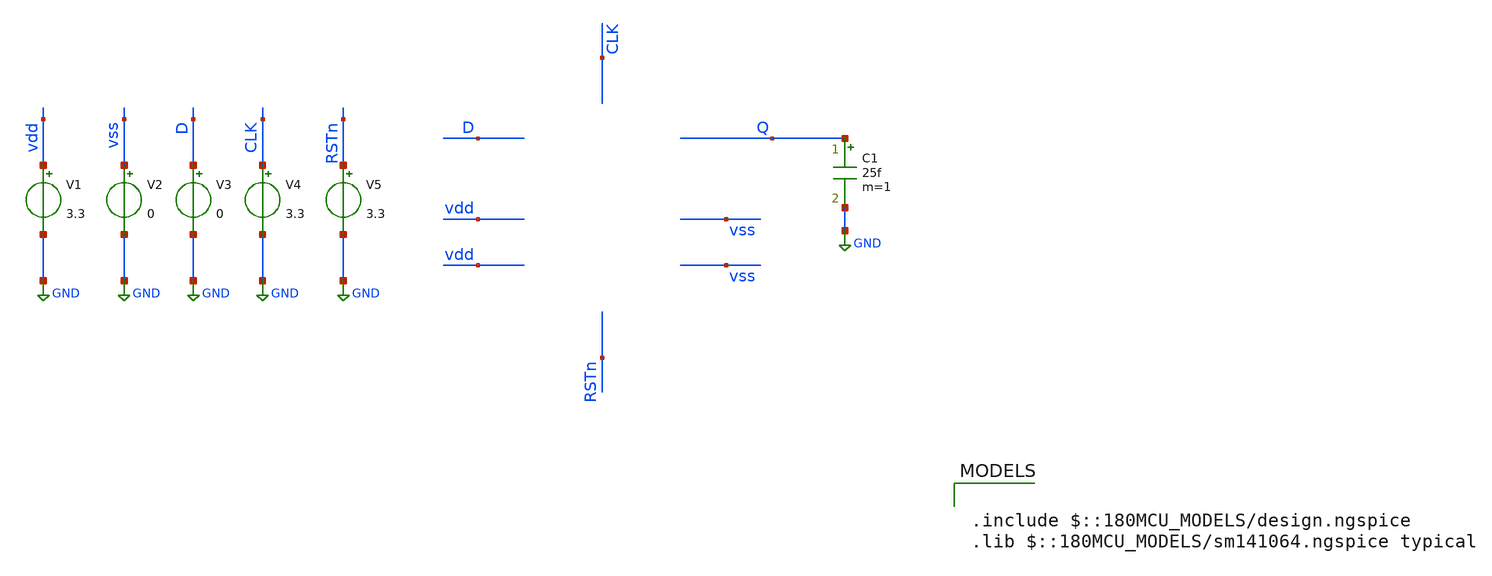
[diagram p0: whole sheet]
** sch_path: dffrnq/dffrnq_postpex_tb.sch
**.subckt dffrnq_postpex_tb
V1 vdd GND 3.3
V2 vss GND 0
V3 D GND 0
V4 CLK GND 3.3
V5 RSTn GND 3.3
C1 Q GND 25f m=1
**** begin user architecture code


.control
save all

** Define input signals
let fsig = 1e3
let tper = 1/fsig
let tper2 = 0.95*tper
let tfr = 0.01*tper
let ton_clk = 0.5*tper - 2*tfr

** Define transient params
let tstop  = 2*tper
let tstep  = 0.001 * tper
let tstop3 = 8*tstop

** --- D waveform: high in 1st+3rd quarters, low in 2nd+4th ---
** Achieve this by making D a square wave whose PERIOD = tstop3/2
** Then it is high for tstop3/4, low for tstop3/4, repeating.
let tper_D = tstop3/2
let ton_D  = 0.5*tper_D - 2*tfr

** --- async reset waveform: high first half, low second half ---
** Make one high pulse that lasts tstop3/2, with a very long period so it doesn't repeat.
let tper_R = 2*tstop3
let ton_R  = 0.5*tstop3 - 2*tfr

** NEW: fast clock independent of fsig
let fclk     = 1e5
let tper_clk = 1/fclk
let tper2clk = 0.95*tper_clk
let tfr_clk  = 0.01*tper_clk
let ton_clk  = 0.5*tper_clk - 2*tfr_clk

** Clock on V4 (unchanged)
alter @v4[PULSE] = [ 0 3.3 0 $&tfr_clk $&tfr_clk $&ton_clk $&tper2clk 0 ]

** D on V3 (quarter pattern across full tstop3)
alter @v3[PULSE] = [ 0 3.3 0 $&tfr $&tfr $&ton_D  $&tper_D 0 ]

** Async reset on V5 (high first half, low second half)
alter @v5[PULSE] = [ 0 3.3 0 $&tfr $&tfr $&ton_R  $&tper_R 0 ]

** Simulation
op
tran $&tstep $&tstop3

plot v(clk) v(d)+5 v(rstn)+10 v(q)+15

** Save waveform
write dff_tb.raw
.endc






.include $::180MCU_MODELS/design.ngspice
.lib $::180MCU_MODELS/sm141064.ngspice typical



* NGSPICE file created from gf180mcu_fd_sc_mcu7t5v0__dffrnq_1.ext - technology: gf180mcuD

.subckt gf180mcu_fd_sc_mcu7t5v0__dffrnq_1 D Q RN VSS CLK VDD VNW VPW
X0 VSS.t2 CLK.t0 a_36_151# VPW.t2 nfet_05v0 ad=0.1053p pd=0.925u as=0.1782p ps=1.69u w=0.405u l=0.6u
X1 VSS.t1 RN.t0 a_1456_156# VPW.t1 nfet_05v0 ad=0.2016p pd=1.48u as=43.2f ps=0.6u w=0.36u l=0.6u
X2 Q.t1 a_2665_112# VDD.t4 VNW.t5 pfet_05v0 ad=0.5346p pd=3.31u as=0.5346p ps=3.31u w=1.215u l=0.5u
X3 a_796_472# D.t0 VSS.t6 VPW.t6 nfet_05v0 ad=93.59999f pd=0.88u as=0.1584p ps=1.6u w=0.36u l=0.6u
X4 VSS.t5 a_2665_112# a_2560_156# VPW.t0 nfet_05v0 ad=0.1224p pd=1.04u as=94.5f ps=0.885u w=0.36u l=0.6u
X5 a_2665_112# a_2248_156# a_3041_156# VPW.t5 nfet_05v0 ad=0.176p pd=1.68u as=0.134p ps=1.1u w=0.4u l=0.6u
X6 a_1000_472# a_448_472# a_796_472# VNW.t13 pfet_05v0 ad=0.2028p pd=1.3u as=0.2028p ps=1.3u w=0.78u l=0.5u
X7 a_2248_156# a_36_151# a_1308_423# VNW.t11 pfet_05v0 ad=0.25375p pd=1.51u as=0.2424p ps=1.465u w=0.505u l=0.5u
X8 a_2248_156# a_448_472# a_1308_423# VPW.t11 nfet_05v0 ad=0.2007p pd=1.475u as=0.2007p ps=1.475u w=0.36u l=0.6u
X9 VDD.t0 CLK.t1 a_36_151# VNW.t0 pfet_05v0 ad=0.2249p pd=1.385u as=0.3806p ps=2.61u w=0.865u l=0.5u
X10 a_1456_156# a_1308_423# a_1288_156# VPW.t7 nfet_05v0 ad=43.2f pd=0.6u as=43.2f ps=0.6u w=0.36u l=0.6u
X11 a_1308_423# a_1000_472# VSS.t3 VPW.t3 nfet_05v0 ad=0.2007p pd=1.475u as=0.2016p ps=1.48u w=0.36u l=0.6u
X12 Q.t0 a_2665_112# VSS.t4 VPW.t4 nfet_05v0 ad=0.3586p pd=2.51u as=0.3586p ps=2.51u w=0.815u l=0.6u
X13 a_448_472# a_36_151# VDD.t9 VNW.t10 pfet_05v0 ad=0.3806p pd=2.61u as=0.2249p ps=1.385u w=0.865u l=0.5u
X14 a_1204_472# a_36_151# a_1000_472# VNW.t9 pfet_05v0 ad=0.2028p pd=1.3u as=0.2028p ps=1.3u w=0.78u l=0.5u
X15 a_1204_472# RN.t1 VDD.t2 VNW.t3 pfet_05v0 ad=0.3432p pd=2.44u as=0.45p ps=2.02u w=0.78u l=0.5u
X16 a_2665_112# RN.t2 VDD.t3 VNW.t2 pfet_05v0 ad=0.26p pd=1.52u as=0.29465p ps=1.74u w=1u l=0.5u
X17 a_2560_156# a_36_151# a_2248_156# VPW.t0 nfet_05v0 ad=94.5f pd=0.885u as=0.2007p ps=1.475u w=0.36u l=0.6u
X18 VDD.t6 a_2248_156# a_2665_112# VNW.t6 pfet_05v0 ad=0.44p pd=2.88u as=0.26p ps=1.52u w=1u l=0.5u
X19 a_1288_156# a_448_472# a_1000_472# VPW.t10 nfet_05v0 ad=43.2f pd=0.6u as=93.59999f ps=0.88u w=0.36u l=0.6u
X20 VDD.t7 a_1308_423# a_1204_472# VNW.t7 pfet_05v0 ad=0.45p pd=2.02u as=0.2028p ps=1.3u w=0.78u l=0.5u
X21 a_2560_156# a_448_472# a_2248_156# VNW.t12 pfet_05v0 ad=0.1313p pd=1.025u as=0.25375p ps=1.51u w=0.505u l=0.5u
X22 a_448_472# a_36_151# VSS.t7 VPW.t9 nfet_05v0 ad=0.1782p pd=1.69u as=0.1053p ps=0.925u w=0.405u l=0.6u
X23 a_3041_156# RN.t3 VSS.t0 VPW.t0 nfet_05v0 ad=0.134p pd=1.1u as=0.1224p ps=1.04u w=0.36u l=0.6u
X24 VDD.t5 a_2665_112# a_2560_156# VNW.t4 pfet_05v0 ad=0.29465p pd=1.74u as=0.1313p ps=1.025u w=0.505u l=0.5u
X25 a_1308_423# a_1000_472# VDD.t1 VNW.t1 pfet_05v0 ad=0.2424p pd=1.465u as=0.2222p ps=1.89u w=0.505u l=0.5u
X26 a_1000_472# a_36_151# a_796_472# VPW.t8 nfet_05v0 ad=93.59999f pd=0.88u as=93.59999f ps=0.88u w=0.36u l=0.6u
X27 a_796_472# D.t1 VDD.t8 VNW.t8 pfet_05v0 ad=0.2028p pd=1.3u as=0.3432p ps=2.44u w=0.78u l=0.5u
R0 CLK.n0 CLK.t0 13.615
R1 CLK.n0 CLK.t1 12.3375
R2 CLK CLK.n0 8.01471
R3 VSS.n5 VSS.t6 11.0252
R4 VSS.n3 VSS.t4 8.92708
R5 VSS.n1 VSS.t3 8.4005
R6 VSS.n1 VSS.t1 8.4005
R7 VSS.n2 VSS.t0 7.3505
R8 VSS.n3 VSS.n2 6.55876
R9 VSS.n6 VSS.n0 6.46615
R10 VSS.n4 VSS.n1 6.43285
R11 VSS.n2 VSS.t5 4.5505
R12 VSS.n0 VSS.t7 4.04494
R13 VSS.n0 VSS.t2 4.04494
R14 VSS.n4 VSS.n3 0.83825
R15 VSS.n5 VSS.n4 0.7895
R16 VSS.n6 VSS.n5 0.2795
R17 VSS VSS.n6 0.0125
R18 VPW.t9 VPW.t6 2760.27
R19 VPW.t1 VPW.t3 2315.07
R20 VPW.t11 VPW.t0 2180.65
R21 VPW.t3 VPW.t11 2031.48
R22 VPW.t8 VPW.t10 1662.1
R23 VPW.t6 VPW.t8 1662.1
R24 VPW.t2 VPW.t9 1662.1
R25 VPW.t7 VPW.t1 1246.58
R26 VPW.t10 VPW.t7 1246.58
R27 VPW VPW.t2 860.731
R28 VPW.n0 VPW.t4 33.9274
R29 VPW.n0 VPW.t5 5.22563
R30 VPW.t0 VPW.n0 3.5722
R31 RN.t3 RN.t0 254.709
R32 RN.n0 RN.t2 31.4493
R33 RN.t0 RN.t1 23.7012
R34 RN RN.n0 8.14503
R35 RN.n0 RN.t3 6.79462
R36 VDD.n5 VDD.t1 9.06272
R37 VDD.n7 VDD.t8 7.70854
R38 VDD.n2 VDD.t5 7.20842
R39 VDD.n4 VDD.n2 5.89642
R40 VDD.n1 VDD.t2 5.38512
R41 VDD.n8 VDD.n0 5.36991
R42 VDD.n6 VDD.n1 5.33285
R43 VDD.n3 VDD.t6 4.66507
R44 VDD.n3 VDD.t4 4.45883
R45 VDD.n1 VDD.t7 4.30819
R46 VDD.n0 VDD.t9 2.10455
R47 VDD.n0 VDD.t0 2.10455
R48 VDD.n2 VDD.t3 1.39717
R49 VDD.n5 VDD.n4 0.78425
R50 VDD.n7 VDD.n6 0.6455
R51 VDD.n6 VDD.n5 0.3125
R52 VDD.n4 VDD.n3 0.3065
R53 VDD.n8 VDD.n7 0.2615
R54 VDD VDD.n8 0.0125
R55 Q Q.t0 8.55859
R56 Q Q.t1 4.30844
R57 VNW.t3 VNW.t1 682.644
R58 VNW.t6 VNW.t5 671.816
R59 VNW.t10 VNW.t8 671.816
R60 VNW.t7 VNW.t3 610.039
R61 VNW.t11 VNW.t12 601.145
R62 VNW.t1 VNW.t11 594.706
R63 VNW.t4 VNW.t2 478.764
R64 VNW.t2 VNW.t6 393.822
R65 VNW.t12 VNW.t4 393.822
R66 VNW.t9 VNW.t7 393.822
R67 VNW.t13 VNW.t9 393.822
R68 VNW.t8 VNW.t13 393.822
R69 VNW.t0 VNW.t10 393.822
R70 VNW VNW.t0 241.314
R71 D.n0 D.t0 13.5573
R72 D.n0 D.t1 11.0235
R73 D D.n0 8.00356
C0 a_2248_156# a_2665_112# 0.63332f
C1 VSS RN 0.44197f
C2 RN a_1308_423# 0.07929f
C3 VSS a_1000_472# 0.04356f
C4 VDD a_2560_156# 0.00217f
C5 a_1000_472# a_1308_423# 0.93419f
C6 RN a_2248_156# 0.09434f
C7 a_2248_156# a_1000_472# 0.00123f
C8 VDD D 0.00937f
C9 VNW a_1204_472# 0.01627f
C10 VDD a_2665_112# 0.10205f
C11 VDD RN 0.03498f
C12 VNW VSS 0.0106f
C13 a_3041_156# a_2665_112# 0.00177f
C14 VNW a_1308_423# 0.14901f
C15 VDD a_1000_472# 0.11921f
C16 VNW a_2248_156# 0.21243f
C17 CLK a_36_151# 0.6696f
C18 a_3041_156# RN 0.01068f
C19 Q VSS 0.1134f
C20 a_36_151# a_796_472# 0.01185f
C21 Q a_2248_156# 0.01436f
C22 VDD VNW 0.50356f
C23 a_1456_156# a_1000_472# 0
C24 a_1000_472# a_1288_156# 0
C25 Q VDD 0.14934f
C26 a_1204_472# a_448_472# 0.009f
C27 VSS a_448_472# 1.20207f
C28 a_448_472# a_1308_423# 0.8821f
C29 a_2248_156# a_448_472# 0.51037f
C30 D a_796_472# 0.08286f
C31 a_36_151# a_2560_156# 0.00367f
C32 VDD a_448_472# 0.45627f
C33 a_1204_472# a_1308_423# 0.02667f
C34 D a_36_151# 0.09411f
C35 a_796_472# a_1000_472# 0.04844f
C36 VSS a_1308_423# 0.01387f
C37 VSS a_2248_156# 0.03047f
C38 a_2248_156# a_1308_423# 0.05672f
C39 a_36_151# a_2665_112# 0.01904f
C40 VNW CLK 0.13704f
C41 RN a_36_151# 0.0801f
C42 a_36_151# a_1000_472# 0.08126f
C43 a_1456_156# a_448_472# 0.00227f
C44 VDD a_1204_472# 0.28263f
C45 VNW a_796_472# 0.01023f
C46 VDD VSS 0.01338f
C47 VDD a_1308_423# 0.09419f
C48 a_448_472# a_1288_156# 0.00207f
C49 VDD a_2248_156# 1.11667f
C50 VNW a_36_151# 1.28833f
C51 VSS a_1456_156# 0.0019f
C52 Q a_36_151# 0
C53 VSS a_1288_156# 0.0017f
C54 a_2665_112# a_2560_156# 0.11606f
C55 RN a_2560_156# 0.03878f
C56 CLK a_448_472# 0.00276f
C57 D a_1000_472# 0
C58 RN a_2665_112# 0.33647f
C59 a_796_472# a_448_472# 0.40164f
C60 RN a_1000_472# 0.0832f
C61 VNW a_2560_156# 0.02016f
C62 a_36_151# a_448_472# 0.53697f
C63 VNW D 0.12823f
C64 VSS CLK 0.02195f
C65 VNW a_2665_112# 0.35472f
C66 VNW RN 0.32949f
C67 VNW a_1000_472# 0.24136f
C68 VSS a_796_472# 0.05215f
C69 Q a_2665_112# 0.10944f
C70 a_36_151# a_1204_472# 0.007f
C71 Q RN 0
C72 VDD CLK 0.02303f
C73 VSS a_36_151# 0.29126f
C74 a_36_151# a_1308_423# 0.05539f
C75 a_2248_156# a_36_151# 0.0428f
C76 VDD a_796_472# 0
C77 Q VNW 0.03444f
C78 VDD a_36_151# 0.41709f
C79 a_448_472# a_2560_156# 0.27749f
C80 D a_448_472# 0.32879f
C81 a_2665_112# a_448_472# 0.02046f
C82 RN a_448_472# 0.07873f
C83 a_1000_472# a_448_472# 0.36196f
C84 VSS a_2560_156# 0.1285f
C85 a_2248_156# a_2560_156# 0.11969f
C86 VSS D 0.06462f
C87 VNW a_448_472# 0.34128f
C88 RN a_1204_472# 0.02104f
C89 a_1000_472# a_1204_472# 0.66083f
C90 VSS a_2665_112# 0.185f
C91 Q VPW 0.11476f
C92 VSS VPW 1.26186f
C93 RN VPW 1.36673f
C94 D VPW 0.25341f
C95 VDD VPW 0.79945f
C96 CLK VPW 0.29124f
C97 VNW VPW 6.1377f
C98 a_2560_156# VPW 0.01697f
C99 a_2665_112# VPW 0.62251f
C100 a_2248_156# VPW 0.37166f
C101 a_1204_472# VPW 0.01297f
C102 a_1000_472# VPW 0.29173f
C103 a_796_472# VPW 0.02321f
C104 a_1308_423# VPW 0.27904f
C105 a_448_472# VPW 0.68441f
C106 a_36_151# VPW 1.43589f
.ends

X1 D Q RSTn vss CLK vdd vdd vss gf180mcu_fd_sc_mcu7t5v0__dffrnq_1



**** end user architecture code
**.ends
.GLOBAL GND
.end
